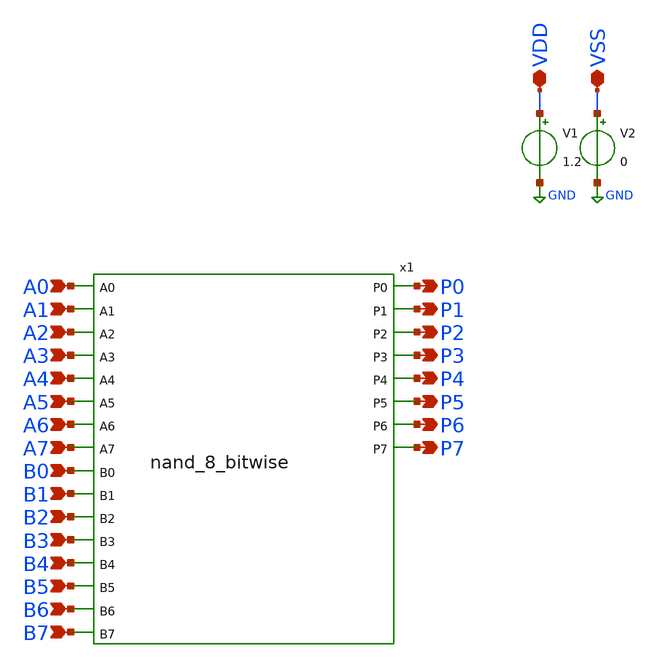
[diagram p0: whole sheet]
** sch_path: design/xschem/NAND/Nand8Tb.sch
**.subckt Nand8Tb VDD VSS A0 A1 B1 A2 B2 A3 B3 A4 B4 A5 B5 A6 B6 A7 B7 B0 P6 P7 P3 P4 P5 P0 P1 P2
*.iopin VDD
*.iopin VSS
*.ipin A0
*.ipin A1
*.ipin B1
*.ipin A2
*.ipin B2
*.ipin A3
*.ipin B3
*.ipin A4
*.ipin B4
*.ipin A5
*.ipin B5
*.ipin A6
*.ipin B6
*.ipin A7
*.ipin B7
*.ipin B0
*.opin P6
*.opin P7
*.opin P3
*.opin P4
*.opin P5
*.opin P0
*.opin P1
*.opin P2
V1 VDD GND 1.2
V2 VSS GND 0
x1 A0 A1 A2 A3 A4 A5 A6 A7 B0 B1 B2 B3 B4 B5 B6 B7 P0 P1 P2 P3 P4 P5 P6 P7 nand_8_bitwise
**** begin user architecture code

** opencircuitdesign pdks install
.lib $::SKYWATER_MODELS/sky130.lib.spice tt_mm





* Parameters
.param period = 4e-08
.param voltage = 1.2
.param end_time = 4e-07
.param tr = 1e-12
.param tf = 1e-12

V_A0 A0 0 PWL(0 0 1e-12 1.2 3.9999e-08 1.2 4e-08 0 4.0001e-08 0 7.9999e-08 0 8e-08 0 8.0001e-08 1.2
+ 1.19999e-07 1.2 1.2e-07 0 1.20001e-07 0 1.5999899999999998e-07 0 1.5999999999999998e-07 0
+ 1.6000099999999998e-07 1.2 1.9999899999999996e-07 1.2 1.9999999999999996e-07 0 2.0000099999999997e-07 0
+ 2.3999899999999995e-07 0 2.399999999999999e-07 0 2.400009999999999e-07 1.2 2.799989999999999e-07 1.2
+ 2.7999999999999986e-07 0 2.8000099999999983e-07 0 3.199989999999998e-07 0 3.199999999999998e-07 0 3.2000099999999977e-07
+ 1.2 3.5999899999999975e-07 1.2 3.5999999999999973e-07 0 3.600009999999997e-07 0 3.999989999999997e-07 0
+ 3.9999999999999966e-07 0)
V_A1 A1 0 PWL(0 0 1e-12 0 3.9999e-08 0 4e-08 0 4.0001e-08 1.2 7.9999e-08 1.2 8e-08 0 8.0001e-08 0
+ 1.19999e-07 0 1.2e-07 0 1.20001e-07 1.2 1.5999899999999998e-07 1.2 1.5999999999999998e-07 0
+ 1.6000099999999998e-07 0 1.9999899999999996e-07 0 1.9999999999999996e-07 0 2.0000099999999997e-07 1.2
+ 2.3999899999999995e-07 1.2 2.399999999999999e-07 0 2.400009999999999e-07 0 2.799989999999999e-07 0 2.7999999999999986e-07
+ 0 2.8000099999999983e-07 1.2 3.199989999999998e-07 1.2 3.199999999999998e-07 0 3.2000099999999977e-07
+ 0 3.5999899999999975e-07 0 3.5999999999999973e-07 0 3.600009999999997e-07 1.2 3.999989999999997e-07
+ 1.2 3.9999999999999966e-07 0)
V_A2 A2 0 PWL(0 0 1e-12 0 3.9999e-08 0 4e-08 0 4.0001e-08 0 7.9999e-08 0 8e-08 0 8.0001e-08 0
+ 1.19999e-07 0 1.2e-07 0 1.20001e-07 0 1.5999899999999998e-07 0 1.5999999999999998e-07 0 1.6000099999999998e-07
+ 0 1.9999899999999996e-07 0 1.9999999999999996e-07 0 2.0000099999999997e-07 0 2.3999899999999995e-07 0
+ 2.399999999999999e-07 0 2.400009999999999e-07 0 2.799989999999999e-07 0 2.7999999999999986e-07 0 2.8000099999999983e-07 0
+ 3.199989999999998e-07 0 3.199999999999998e-07 0 3.2000099999999977e-07 0 3.5999899999999975e-07 0 3.5999999999999973e-07
+ 0 3.600009999999997e-07 0 3.999989999999997e-07 0 3.9999999999999966e-07 0 4.0000099999999964e-07 0
+ 4.399989999999996e-07 0 4.399999999999996e-07 0)
V_A3 A3 0 PWL(0 0 1e-12 0 3.9999e-08 0 4e-08 0 4.0001e-08 0 7.9999e-08 0 8e-08 0 8.0001e-08 0
+ 1.19999e-07 0 1.2e-07 0 1.20001e-07 0 1.5999899999999998e-07 0 1.5999999999999998e-07 0 1.6000099999999998e-07
+ 0 1.9999899999999996e-07 0 1.9999999999999996e-07 0 2.0000099999999997e-07 0 2.3999899999999995e-07 0
+ 2.399999999999999e-07 0 2.400009999999999e-07 0 2.799989999999999e-07 0 2.7999999999999986e-07 0 2.8000099999999983e-07 0
+ 3.199989999999998e-07 0 3.199999999999998e-07 0 3.2000099999999977e-07 0 3.5999899999999975e-07 0 3.5999999999999973e-07
+ 0 3.600009999999997e-07 0 3.999989999999997e-07 0 3.9999999999999966e-07 0 4.0000099999999964e-07 0
+ 4.399989999999996e-07 0 4.399999999999996e-07 0)
V_A4 A4 0 PWL(0 0 1e-12 0 3.9999e-08 0 4e-08 0 4.0001e-08 0 7.9999e-08 0 8e-08 0 8.0001e-08 0
+ 1.19999e-07 0 1.2e-07 0 1.20001e-07 0 1.5999899999999998e-07 0 1.5999999999999998e-07 0 1.6000099999999998e-07
+ 0 1.9999899999999996e-07 0 1.9999999999999996e-07 0 2.0000099999999997e-07 0 2.3999899999999995e-07 0
+ 2.399999999999999e-07 0 2.400009999999999e-07 0 2.799989999999999e-07 0 2.7999999999999986e-07 0 2.8000099999999983e-07 0
+ 3.199989999999998e-07 0 3.199999999999998e-07 0 3.2000099999999977e-07 0 3.5999899999999975e-07 0 3.5999999999999973e-07
+ 0 3.600009999999997e-07 0 3.999989999999997e-07 0 3.9999999999999966e-07 0 4.0000099999999964e-07 0
+ 4.399989999999996e-07 0 4.399999999999996e-07 0)
V_A5 A5 0 PWL(0 0 1e-12 0 3.9999e-08 0 4e-08 0 4.0001e-08 0 7.9999e-08 0 8e-08 0 8.0001e-08 0
+ 1.19999e-07 0 1.2e-07 0 1.20001e-07 0 1.5999899999999998e-07 0 1.5999999999999998e-07 0 1.6000099999999998e-07
+ 0 1.9999899999999996e-07 0 1.9999999999999996e-07 0 2.0000099999999997e-07 0 2.3999899999999995e-07 0
+ 2.399999999999999e-07 0 2.400009999999999e-07 0 2.799989999999999e-07 0 2.7999999999999986e-07 0 2.8000099999999983e-07 0
+ 3.199989999999998e-07 0 3.199999999999998e-07 0 3.2000099999999977e-07 0 3.5999899999999975e-07 0 3.5999999999999973e-07
+ 0 3.600009999999997e-07 0 3.999989999999997e-07 0 3.9999999999999966e-07 0 4.0000099999999964e-07 0
+ 4.399989999999996e-07 0 4.399999999999996e-07 0)
V_A6 A6 0 PWL(0 0 1e-12 0 3.9999e-08 0 4e-08 0 4.0001e-08 0 7.9999e-08 0 8e-08 0 8.0001e-08 0
+ 1.19999e-07 0 1.2e-07 0 1.20001e-07 0 1.5999899999999998e-07 0 1.5999999999999998e-07 0 1.6000099999999998e-07
+ 0 1.9999899999999996e-07 0 1.9999999999999996e-07 0 2.0000099999999997e-07 0 2.3999899999999995e-07 0
+ 2.399999999999999e-07 0 2.400009999999999e-07 0 2.799989999999999e-07 0 2.7999999999999986e-07 0 2.8000099999999983e-07 0
+ 3.199989999999998e-07 0 3.199999999999998e-07 0 3.2000099999999977e-07 0 3.5999899999999975e-07 0 3.5999999999999973e-07
+ 0 3.600009999999997e-07 0 3.999989999999997e-07 0 3.9999999999999966e-07 0 4.0000099999999964e-07 0
+ 4.399989999999996e-07 0 4.399999999999996e-07 0)
V_A7 A7 0 PWL(0 0 1e-12 0 3.9999e-08 0 4e-08 0 4.0001e-08 0 7.9999e-08 0 8e-08 0 8.0001e-08 0
+ 1.19999e-07 0 1.2e-07 0 1.20001e-07 0 1.5999899999999998e-07 0 1.5999999999999998e-07 0 1.6000099999999998e-07
+ 0 1.9999899999999996e-07 0 1.9999999999999996e-07 0 2.0000099999999997e-07 0 2.3999899999999995e-07 0
+ 2.399999999999999e-07 0 2.400009999999999e-07 0 2.799989999999999e-07 0 2.7999999999999986e-07 0 2.8000099999999983e-07 0
+ 3.199989999999998e-07 0 3.199999999999998e-07 0 3.2000099999999977e-07 0 3.5999899999999975e-07 0 3.5999999999999973e-07
+ 0 3.600009999999997e-07 0 3.999989999999997e-07 0 3.9999999999999966e-07 0 4.0000099999999964e-07 0
+ 4.399989999999996e-07 0 4.399999999999996e-07 0)
V_B0 B0 0 PWL(0 0 1e-12 0 3.9999e-08 0 4e-08 0 4.0001e-08 0 7.9999e-08 0 8e-08 0 8.0001e-08 1.2
+ 1.19999e-07 1.2 1.2e-07 0 1.20001e-07 1.2 1.5999899999999998e-07 1.2 1.5999999999999998e-07 0
+ 1.6000099999999998e-07 0 1.9999899999999996e-07 0 1.9999999999999996e-07 0 2.0000099999999997e-07 0 2.3999899999999995e-07
+ 0 2.399999999999999e-07 0 2.400009999999999e-07 1.2 2.799989999999999e-07 1.2 2.7999999999999986e-07
+ 0 2.8000099999999983e-07 1.2 3.199989999999998e-07 1.2 3.199999999999998e-07 0 3.2000099999999977e-07
+ 0 3.5999899999999975e-07 0 3.5999999999999973e-07 0 3.600009999999997e-07 0 3.999989999999997e-07 0
+ 3.9999999999999966e-07 0)
V_B1 B1 0 PWL(0 0 1e-12 1.2 3.9999e-08 1.2 4e-08 0 4.0001e-08 1.2 7.9999e-08 1.2 8e-08 0 8.0001e-08
+ 0 1.19999e-07 0 1.2e-07 0 1.20001e-07 0 1.5999899999999998e-07 0 1.5999999999999998e-07 0
+ 1.6000099999999998e-07 1.2 1.9999899999999996e-07 1.2 1.9999999999999996e-07 0 2.0000099999999997e-07 1.2
+ 2.3999899999999995e-07 1.2 2.399999999999999e-07 0 2.400009999999999e-07 0 2.799989999999999e-07 0 2.7999999999999986e-07
+ 0 2.8000099999999983e-07 0 3.199989999999998e-07 0 3.199999999999998e-07 0 3.2000099999999977e-07 1.2
+ 3.5999899999999975e-07 1.2 3.5999999999999973e-07 0 3.600009999999997e-07 1.2 3.999989999999997e-07 1.2
+ 3.9999999999999966e-07 0)
V_B2 B2 0 PWL(0 0 1e-12 0 3.9999e-08 0 4e-08 0 4.0001e-08 0 7.9999e-08 0 8e-08 0 8.0001e-08 0
+ 1.19999e-07 0 1.2e-07 0 1.20001e-07 0 1.5999899999999998e-07 0 1.5999999999999998e-07 0 1.6000099999999998e-07
+ 0 1.9999899999999996e-07 0 1.9999999999999996e-07 0 2.0000099999999997e-07 0 2.3999899999999995e-07 0
+ 2.399999999999999e-07 0 2.400009999999999e-07 0 2.799989999999999e-07 0 2.7999999999999986e-07 0 2.8000099999999983e-07 0
+ 3.199989999999998e-07 0 3.199999999999998e-07 0 3.2000099999999977e-07 0 3.5999899999999975e-07 0 3.5999999999999973e-07
+ 0 3.600009999999997e-07 0 3.999989999999997e-07 0 3.9999999999999966e-07 0 4.0000099999999964e-07 0
+ 4.399989999999996e-07 0 4.399999999999996e-07 0)
V_B3 B3 0 PWL(0 0 1e-12 0 3.9999e-08 0 4e-08 0 4.0001e-08 0 7.9999e-08 0 8e-08 0 8.0001e-08 0
+ 1.19999e-07 0 1.2e-07 0 1.20001e-07 0 1.5999899999999998e-07 0 1.5999999999999998e-07 0 1.6000099999999998e-07
+ 0 1.9999899999999996e-07 0 1.9999999999999996e-07 0 2.0000099999999997e-07 0 2.3999899999999995e-07 0
+ 2.399999999999999e-07 0 2.400009999999999e-07 0 2.799989999999999e-07 0 2.7999999999999986e-07 0 2.8000099999999983e-07 0
+ 3.199989999999998e-07 0 3.199999999999998e-07 0 3.2000099999999977e-07 0 3.5999899999999975e-07 0 3.5999999999999973e-07
+ 0 3.600009999999997e-07 0 3.999989999999997e-07 0 3.9999999999999966e-07 0 4.0000099999999964e-07 0
+ 4.399989999999996e-07 0 4.399999999999996e-07 0)
V_B4 B4 0 PWL(0 0 1e-12 0 3.9999e-08 0 4e-08 0 4.0001e-08 0 7.9999e-08 0 8e-08 0 8.0001e-08 0
+ 1.19999e-07 0 1.2e-07 0 1.20001e-07 0 1.5999899999999998e-07 0 1.5999999999999998e-07 0 1.6000099999999998e-07
+ 0 1.9999899999999996e-07 0 1.9999999999999996e-07 0 2.0000099999999997e-07 0 2.3999899999999995e-07 0
+ 2.399999999999999e-07 0 2.400009999999999e-07 0 2.799989999999999e-07 0 2.7999999999999986e-07 0 2.8000099999999983e-07 0
+ 3.199989999999998e-07 0 3.199999999999998e-07 0 3.2000099999999977e-07 0 3.5999899999999975e-07 0 3.5999999999999973e-07
+ 0 3.600009999999997e-07 0 3.999989999999997e-07 0 3.9999999999999966e-07 0 4.0000099999999964e-07 0
+ 4.399989999999996e-07 0 4.399999999999996e-07 0)
V_B5 B5 0 PWL(0 0 1e-12 0 3.9999e-08 0 4e-08 0 4.0001e-08 0 7.9999e-08 0 8e-08 0 8.0001e-08 0
+ 1.19999e-07 0 1.2e-07 0 1.20001e-07 0 1.5999899999999998e-07 0 1.5999999999999998e-07 0 1.6000099999999998e-07
+ 0 1.9999899999999996e-07 0 1.9999999999999996e-07 0 2.0000099999999997e-07 0 2.3999899999999995e-07 0
+ 2.399999999999999e-07 0 2.400009999999999e-07 0 2.799989999999999e-07 0 2.7999999999999986e-07 0 2.8000099999999983e-07 0
+ 3.199989999999998e-07 0 3.199999999999998e-07 0 3.2000099999999977e-07 0 3.5999899999999975e-07 0 3.5999999999999973e-07
+ 0 3.600009999999997e-07 0 3.999989999999997e-07 0 3.9999999999999966e-07 0 4.0000099999999964e-07 0
+ 4.399989999999996e-07 0 4.399999999999996e-07 0)
V_B6 B6 0 PWL(0 0 1e-12 0 3.9999e-08 0 4e-08 0 4.0001e-08 0 7.9999e-08 0 8e-08 0 8.0001e-08 0
+ 1.19999e-07 0 1.2e-07 0 1.20001e-07 0 1.5999899999999998e-07 0 1.5999999999999998e-07 0 1.6000099999999998e-07
+ 0 1.9999899999999996e-07 0 1.9999999999999996e-07 0 2.0000099999999997e-07 0 2.3999899999999995e-07 0
+ 2.399999999999999e-07 0 2.400009999999999e-07 0 2.799989999999999e-07 0 2.7999999999999986e-07 0 2.8000099999999983e-07 0
+ 3.199989999999998e-07 0 3.199999999999998e-07 0 3.2000099999999977e-07 0 3.5999899999999975e-07 0 3.5999999999999973e-07
+ 0 3.600009999999997e-07 0 3.999989999999997e-07 0 3.9999999999999966e-07 0 4.0000099999999964e-07 0
+ 4.399989999999996e-07 0 4.399999999999996e-07 0)
V_B7 B7 0 PWL(0 0 1e-12 0 3.9999e-08 0 4e-08 0 4.0001e-08 0 7.9999e-08 0 8e-08 0 8.0001e-08 0
+ 1.19999e-07 0 1.2e-07 0 1.20001e-07 0 1.5999899999999998e-07 0 1.5999999999999998e-07 0 1.6000099999999998e-07
+ 0 1.9999899999999996e-07 0 1.9999999999999996e-07 0 2.0000099999999997e-07 0 2.3999899999999995e-07 0
+ 2.399999999999999e-07 0 2.400009999999999e-07 0 2.799989999999999e-07 0 2.7999999999999986e-07 0 2.8000099999999983e-07 0
+ 3.199989999999998e-07 0 3.199999999999998e-07 0 3.2000099999999977e-07 0 3.5999899999999975e-07 0 3.5999999999999973e-07
+ 0 3.600009999999997e-07 0 3.999989999999997e-07 0 3.9999999999999966e-07 0 4.0000099999999964e-07 0
+ 4.399989999999996e-07 0 4.399999999999996e-07 0)
* Control block for transient simulation
.control
tran 1ns 400ns           ; Run transient simulation from 0 to 400ns with 1ns time step

* Plot the output signals P0 to P7
plot V(A0) V(A1) V(A2) V(A3) V(A4) V(A5) V(A6) V(A7)
plot V(B0) V(B1) V(B2) V(B3) V(B4) V(B5) V(B6) V(B7)
plot V(P0) V(P1) V(P2) V(P3) V(P4) V(P5) V(P6) V(P7)

.endc




**** end user architecture code
**.ends

* expanding   symbol:  NAND/nand_8_bitwise.sym # of pins=24
** sym_path: design/xschem/NAND/nand_8_bitwise.sym
** sch_path: design/xschem/NAND/nand_8_bitwise.sch
.subckt nand_8_bitwise A0 A1 A2 A3 A4 A5 A6 A7 B0 B1 B2 B3 B4 B5 B6 B7 P0 P1 P2 P3 P4 P5 P6 P7
*.ipin B7
*.ipin B5
*.ipin B6
*.ipin B4
*.ipin B3
*.ipin B2
*.ipin B1
*.ipin B0
*.opin P7
*.opin P6
*.opin P5
*.opin P4
*.opin P3
*.opin P2
*.opin P1
*.opin P0
*.ipin A7
*.ipin A5
*.ipin A6
*.ipin A4
*.ipin A3
*.ipin A2
*.ipin A1
*.ipin A0
x1 B7 A7 VSS VDD P7 nand2
x2 B6 A6 VSS VDD P6 nand2
x3 B5 A5 VSS VDD P5 nand2
x4 B4 A4 VSS VDD P4 nand2
x5 B3 A3 VSS VDD P3 nand2
x6 B2 A2 VSS VDD P2 nand2
x7 B1 A1 VSS VDD P1 nand2
x8 B0 A0 VSS VDD P0 nand2
.ends


* expanding   symbol:  NAND/nand2.sym # of pins=3
** sym_path: design/xschem/NAND/nand2.sym
** sch_path: design/xschem/NAND/nand2.sch
.subckt nand2 A B VSS VDD Y
*.ipin A
*.opin Y
*.ipin B
XM1 Y A VDD VDD sky130_fd_pr__pfet_01v8 L=0.15 W=3.2 nf=1 ad='int((nf+1)/2) * W/nf * 0.29' as='int((nf+2)/2) * W/nf * 0.29'
+ pd='2*int((nf+1)/2) * (W/nf + 0.29)' ps='2*int((nf+2)/2) * (W/nf + 0.29)' nrd='0.29 / W' nrs='0.29 / W'
+ sa=0 sb=0 sd=0 mult=1 m=1
XM2 Y A net1 net1 sky130_fd_pr__nfet_01v8 L=0.15 W=2 nf=1 ad='int((nf+1)/2) * W/nf * 0.29' as='int((nf+2)/2) * W/nf * 0.29'
+ pd='2*int((nf+1)/2) * (W/nf + 0.29)' ps='2*int((nf+2)/2) * (W/nf + 0.29)' nrd='0.29 / W' nrs='0.29 / W'
+ sa=0 sb=0 sd=0 mult=1 m=1
XM3 net1 B VSS VSS sky130_fd_pr__nfet_01v8 L=0.15 W=2 nf=1 ad='int((nf+1)/2) * W/nf * 0.29' as='int((nf+2)/2) * W/nf * 0.29'
+ pd='2*int((nf+1)/2) * (W/nf + 0.29)' ps='2*int((nf+2)/2) * (W/nf + 0.29)' nrd='0.29 / W' nrs='0.29 / W'
+ sa=0 sb=0 sd=0 mult=1 m=1
XM4 Y B VDD VDD sky130_fd_pr__pfet_01v8 L=0.15 W=3.2 nf=1 ad='int((nf+1)/2) * W/nf * 0.29' as='int((nf+2)/2) * W/nf * 0.29'
+ pd='2*int((nf+1)/2) * (W/nf + 0.29)' ps='2*int((nf+2)/2) * (W/nf + 0.29)' nrd='0.29 / W' nrs='0.29 / W'
+ sa=0 sb=0 sd=0 mult=1 m=1
.ends

.GLOBAL GND
.end
